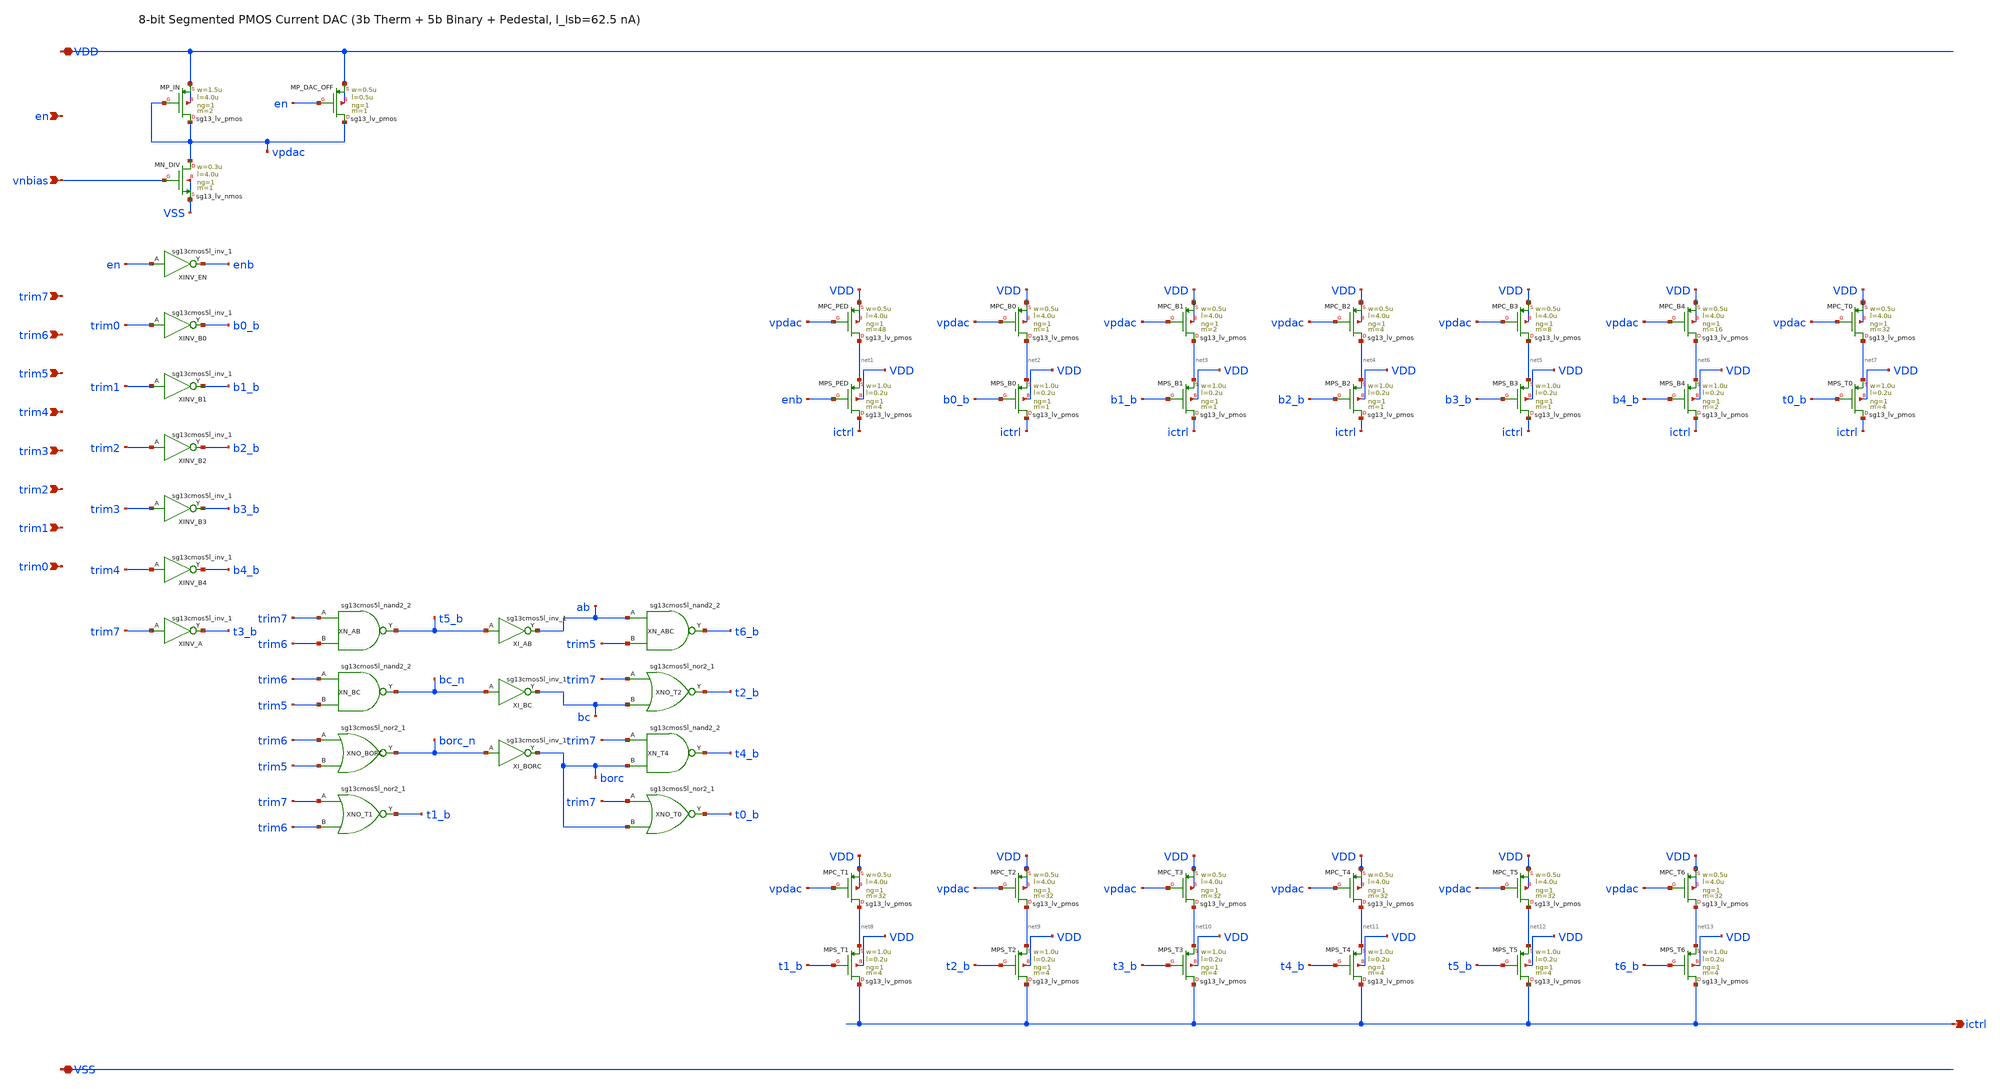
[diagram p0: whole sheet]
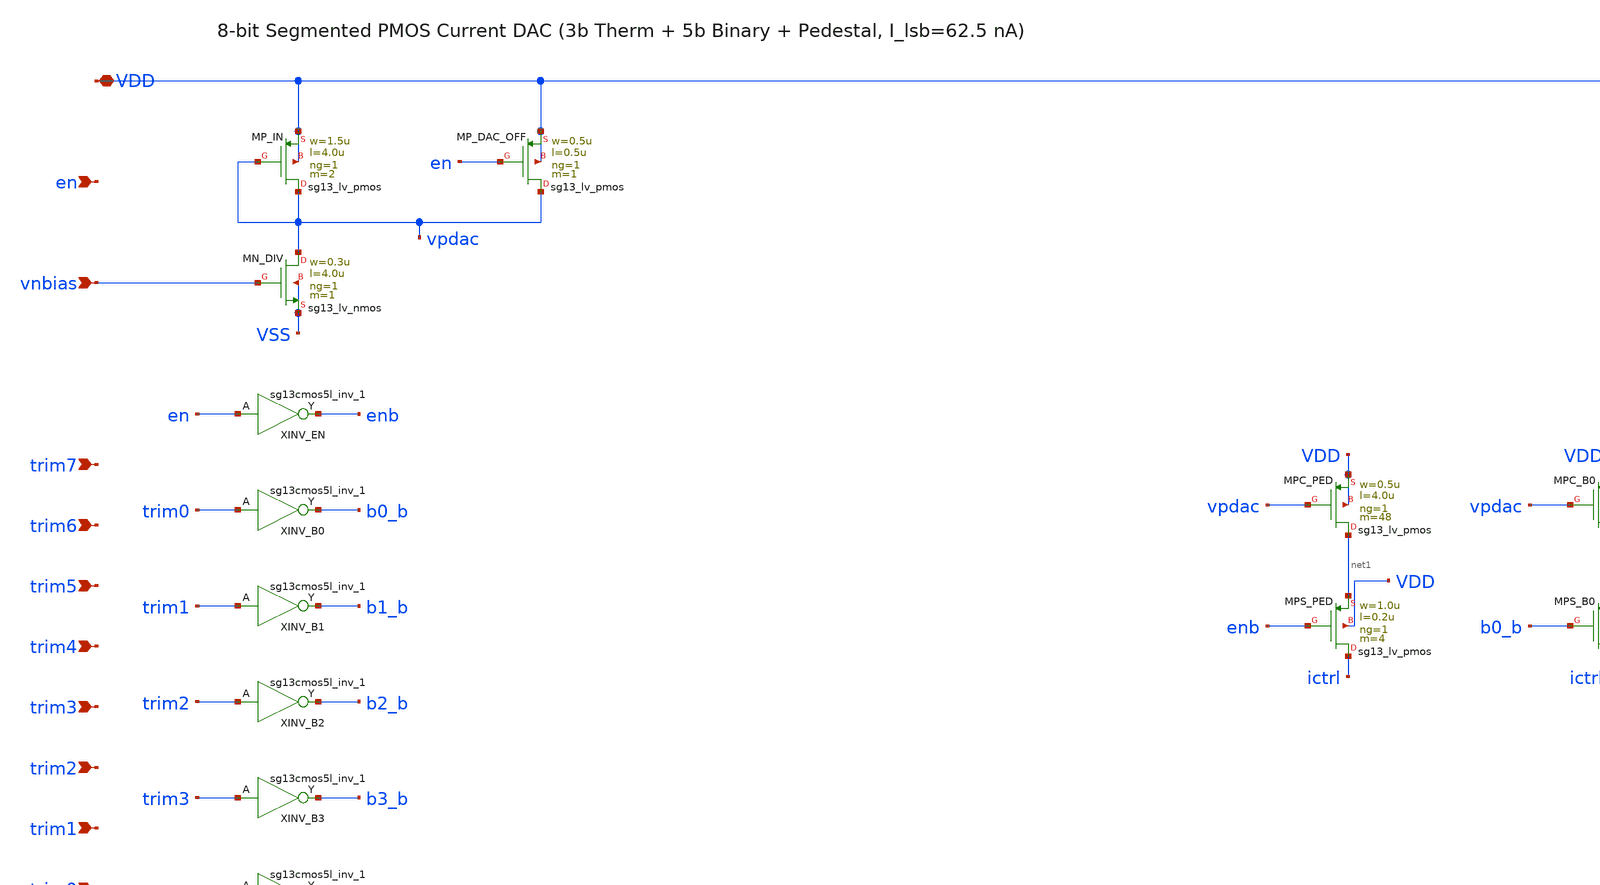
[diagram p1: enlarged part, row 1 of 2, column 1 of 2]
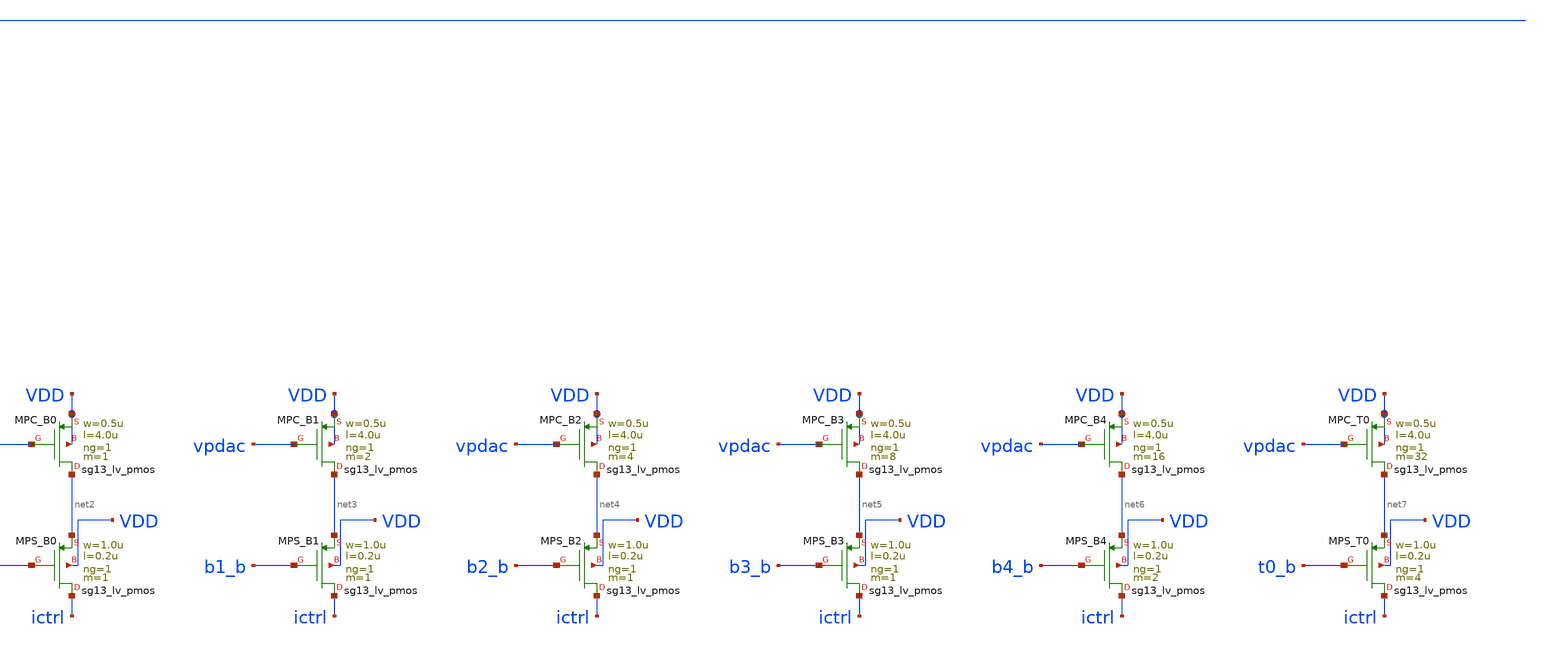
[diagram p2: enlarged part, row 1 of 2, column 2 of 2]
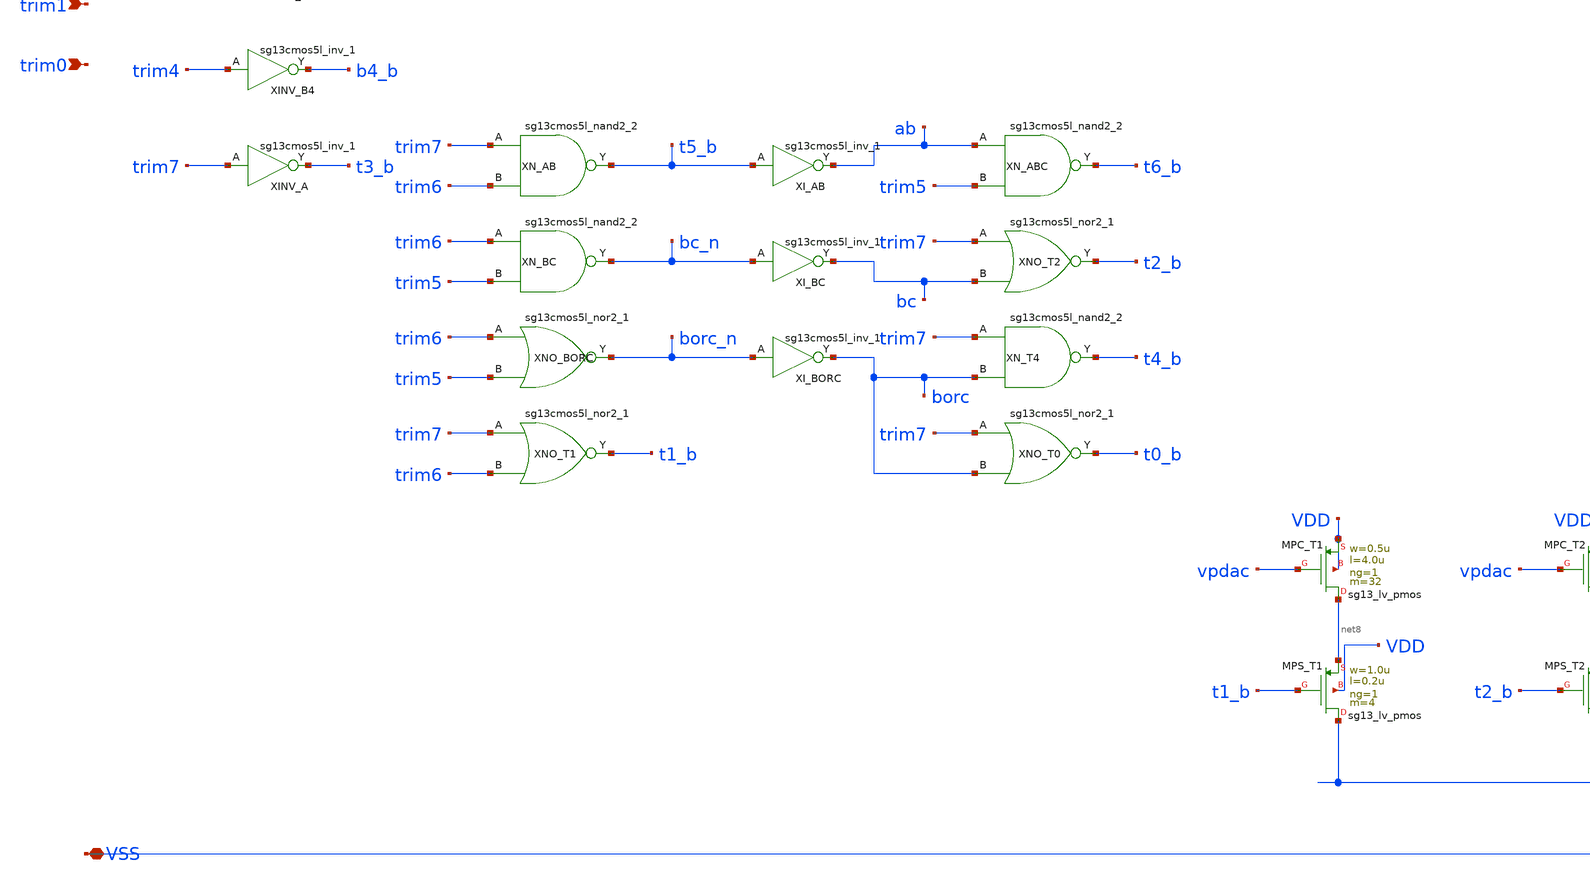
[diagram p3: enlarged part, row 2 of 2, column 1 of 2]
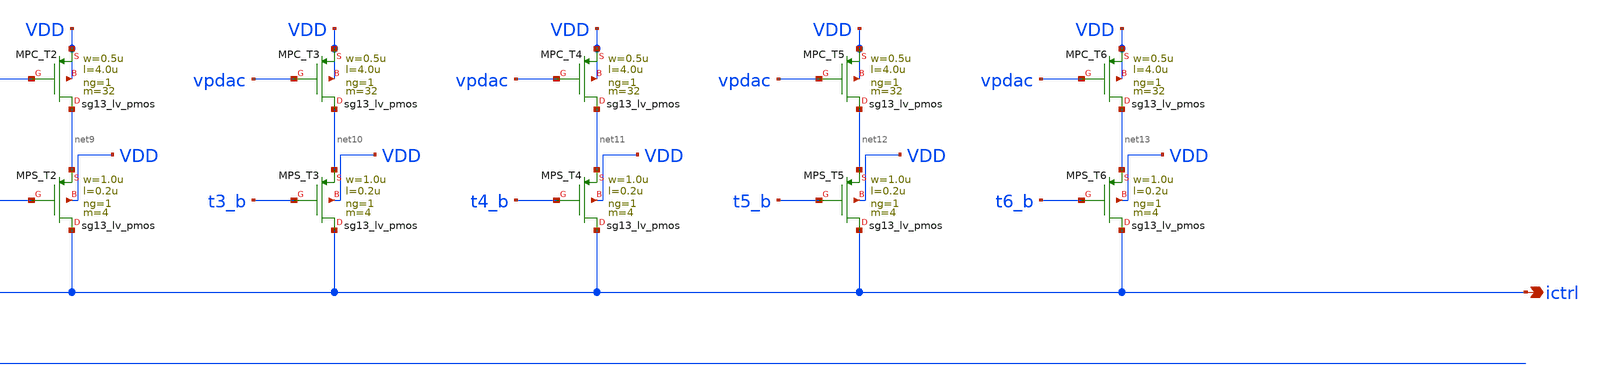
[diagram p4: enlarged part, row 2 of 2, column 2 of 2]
** sch_path: analog/osc_ring_cc/idac_8b.sch
**.subckt idac_8b VDD VSS en vnbias trim7 trim6 trim5 trim4 trim3 trim2 trim1 trim0 ictrl
*.iopin VDD
*.iopin VSS
*.ipin en
*.ipin vnbias
*.ipin trim7
*.ipin trim6
*.ipin trim5
*.ipin trim4
*.ipin trim3
*.ipin trim2
*.ipin trim1
*.ipin trim0
*.opin ictrl
XMN_DIV vpdac vnbias VSS VSS sg13_lv_nmos w=0.3u l=4.0u ng=1 m=1 mm_ok=1
XMP_IN vpdac vpdac VDD VDD sg13_lv_pmos w=1.5u l=4.0u ng=1 m=2 mm_ok=1
XMP_DAC_OFF vpdac en VDD VDD sg13_lv_pmos w=0.5u l=0.5u ng=1 m=1 mm_ok=1
XINV_EN enb en VDD VSS sg13cmos5l_inv_1
XINV_B0 b0_b trim0 VDD VSS sg13cmos5l_inv_1
XINV_B1 b1_b trim1 VDD VSS sg13cmos5l_inv_1
XINV_B2 b2_b trim2 VDD VSS sg13cmos5l_inv_1
XINV_B3 b3_b trim3 VDD VSS sg13cmos5l_inv_1
XINV_B4 b4_b trim4 VDD VSS sg13cmos5l_inv_1
XINV_A t3_b trim7 VDD VSS sg13cmos5l_inv_1
XN_AB t5_b trim7 trim6 VDD VSS sg13cmos5l_nand2_2
XI_AB ab t5_b VDD VSS sg13cmos5l_inv_1
XN_ABC t6_b ab trim5 VDD VSS sg13cmos5l_nand2_2
XN_BC bc_n trim6 trim5 VDD VSS sg13cmos5l_nand2_2
XI_BC bc bc_n VDD VSS sg13cmos5l_inv_1
XNO_T2 t2_b trim7 bc VDD VSS sg13cmos5l_nor2_1
XNO_BORC borc_n trim6 trim5 VDD VSS sg13cmos5l_nor2_1
XI_BORC borc borc_n VDD VSS sg13cmos5l_inv_1
XN_T4 t4_b trim7 borc VDD VSS sg13cmos5l_nand2_2
XNO_T1 t1_b trim7 trim6 VDD VSS sg13cmos5l_nor2_1
XNO_T0 t0_b trim7 borc VDD VSS sg13cmos5l_nor2_1
XMPC_PED net1 vpdac VDD VDD sg13_lv_pmos w=0.5u l=4.0u ng=1 m=48 mm_ok=1
XMPS_PED ictrl enb net1 VDD sg13_lv_pmos w=1.0u l=0.2u ng=1 m=4 mm_ok=1
XMPC_B0 net2 vpdac VDD VDD sg13_lv_pmos w=0.5u l=4.0u ng=1 m=1 mm_ok=1
XMPS_B0 ictrl b0_b net2 VDD sg13_lv_pmos w=1.0u l=0.2u ng=1 m=1 mm_ok=1
XMPC_B1 net3 vpdac VDD VDD sg13_lv_pmos w=0.5u l=4.0u ng=1 m=2 mm_ok=1
XMPS_B1 ictrl b1_b net3 VDD sg13_lv_pmos w=1.0u l=0.2u ng=1 m=1 mm_ok=1
XMPC_B2 net4 vpdac VDD VDD sg13_lv_pmos w=0.5u l=4.0u ng=1 m=4 mm_ok=1
XMPS_B2 ictrl b2_b net4 VDD sg13_lv_pmos w=1.0u l=0.2u ng=1 m=1 mm_ok=1
XMPC_B3 net5 vpdac VDD VDD sg13_lv_pmos w=0.5u l=4.0u ng=1 m=8 mm_ok=1
XMPS_B3 ictrl b3_b net5 VDD sg13_lv_pmos w=1.0u l=0.2u ng=1 m=1 mm_ok=1
XMPC_B4 net6 vpdac VDD VDD sg13_lv_pmos w=0.5u l=4.0u ng=1 m=16 mm_ok=1
XMPS_B4 ictrl b4_b net6 VDD sg13_lv_pmos w=1.0u l=0.2u ng=1 m=2 mm_ok=1
XMPC_T0 net7 vpdac VDD VDD sg13_lv_pmos w=0.5u l=4.0u ng=1 m=32 mm_ok=1
XMPS_T0 ictrl t0_b net7 VDD sg13_lv_pmos w=1.0u l=0.2u ng=1 m=4 mm_ok=1
XMPC_T1 net8 vpdac VDD VDD sg13_lv_pmos w=0.5u l=4.0u ng=1 m=32 mm_ok=1
XMPS_T1 ictrl t1_b net8 VDD sg13_lv_pmos w=1.0u l=0.2u ng=1 m=4 mm_ok=1
XMPC_T2 net9 vpdac VDD VDD sg13_lv_pmos w=0.5u l=4.0u ng=1 m=32 mm_ok=1
XMPS_T2 ictrl t2_b net9 VDD sg13_lv_pmos w=1.0u l=0.2u ng=1 m=4 mm_ok=1
XMPC_T3 net10 vpdac VDD VDD sg13_lv_pmos w=0.5u l=4.0u ng=1 m=32 mm_ok=1
XMPS_T3 ictrl t3_b net10 VDD sg13_lv_pmos w=1.0u l=0.2u ng=1 m=4 mm_ok=1
XMPC_T4 net11 vpdac VDD VDD sg13_lv_pmos w=0.5u l=4.0u ng=1 m=32 mm_ok=1
XMPS_T4 ictrl t4_b net11 VDD sg13_lv_pmos w=1.0u l=0.2u ng=1 m=4 mm_ok=1
XMPC_T5 net12 vpdac VDD VDD sg13_lv_pmos w=0.5u l=4.0u ng=1 m=32 mm_ok=1
XMPS_T5 ictrl t5_b net12 VDD sg13_lv_pmos w=1.0u l=0.2u ng=1 m=4 mm_ok=1
XMPC_T6 net13 vpdac VDD VDD sg13_lv_pmos w=0.5u l=4.0u ng=1 m=32 mm_ok=1
XMPS_T6 ictrl t6_b net13 VDD sg13_lv_pmos w=1.0u l=0.2u ng=1 m=4 mm_ok=1
**.ends
.end
